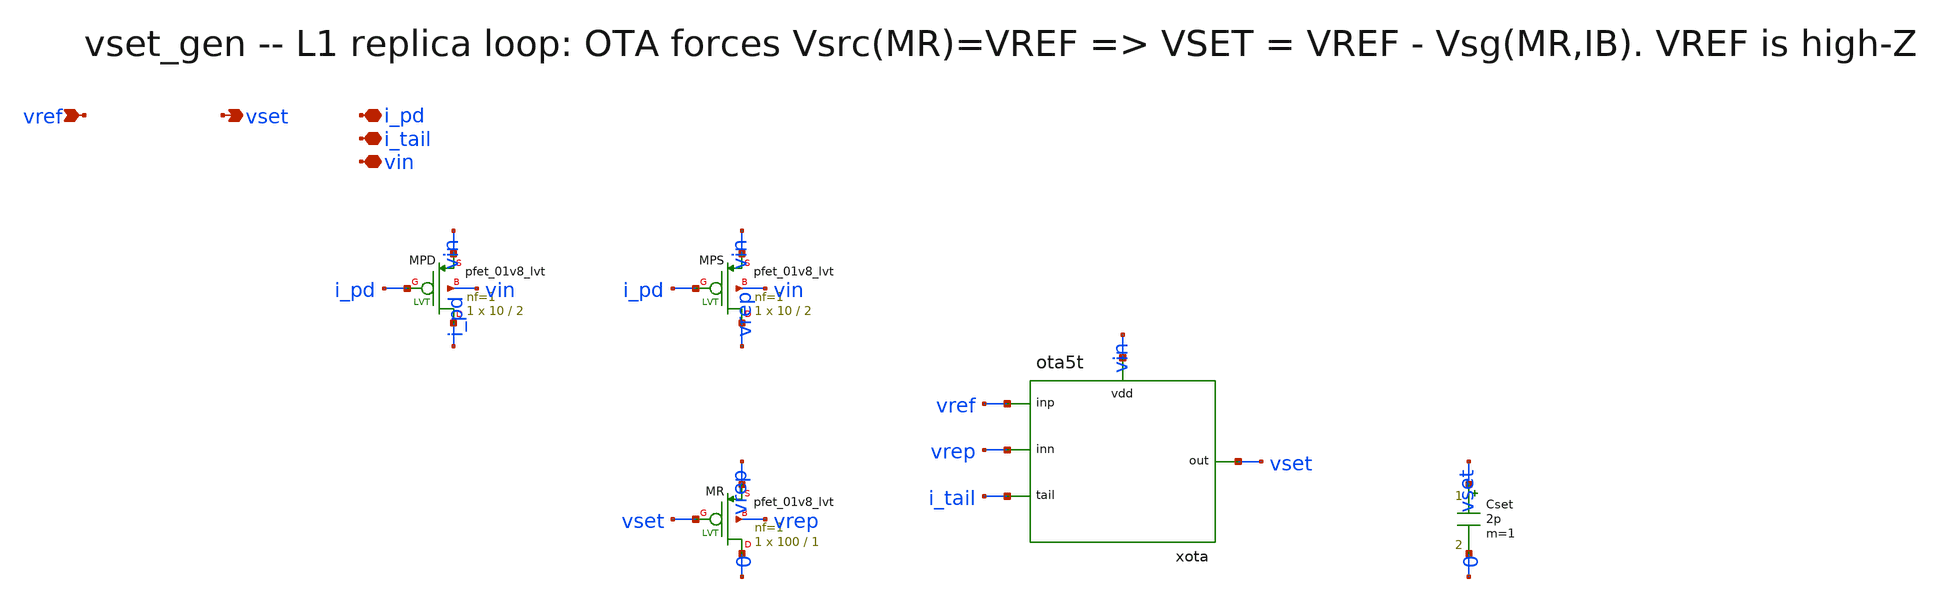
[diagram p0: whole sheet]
** sch_path: xschem/onetops/vset_gen.sch
**.subckt vset_gen vref vset i_pd i_tail vin
*.ipin vref
*.opin vset
*.iopin i_pd
*.iopin i_tail
*.iopin vin
XMPD i_pd i_pd vin vin sky130_fd_pr__pfet_01v8_lvt L=2 W=10 nf=1 ad='int((1 + 1)/2) * 10 / 1 * 0.29'
+ as='int((1 + 2)/2) * 10 / 1 * 0.29' pd='2*int((1 + 1)/2) * (10 / 1 + 0.29)' ps='2*int((1 + 2)/2) * (10 / 1 + 0.29)'
+ nrd='0.29 / 10 ' nrs='0.29 / 10 ' sa=0 sb=0 sd=0 mult=1 m=1
XMPS vrep i_pd vin vin sky130_fd_pr__pfet_01v8_lvt L=2 W=10 nf=1 ad='int((1 + 1)/2) * 10 / 1 * 0.29'
+ as='int((1 + 2)/2) * 10 / 1 * 0.29' pd='2*int((1 + 1)/2) * (10 / 1 + 0.29)' ps='2*int((1 + 2)/2) * (10 / 1 + 0.29)'
+ nrd='0.29 / 10 ' nrs='0.29 / 10 ' sa=0 sb=0 sd=0 mult=1 m=1
XMR 0 vset vrep vrep sky130_fd_pr__pfet_01v8_lvt L=1 W=100 nf=1 ad='int((1 + 1)/2) * 100 / 1 * 0.29'
+ as='int((1 + 2)/2) * 100 / 1 * 0.29' pd='2*int((1 + 1)/2) * (100 / 1 + 0.29)' ps='2*int((1 + 2)/2) * (100 / 1 + 0.29)'
+ nrd='0.29 / 100 ' nrs='0.29 / 100 ' sa=0 sb=0 sd=0 mult=1 m=1
xota vref vrep i_tail vset vin ota5t
Cset vset 0 2p m=1
**.ends

* expanding   symbol:  onetops/ota5t.sym # of pins=5
** sym_path: xschem/onetops/ota5t.sym
** sch_path: xschem/onetops/ota5t.sch
.subckt ota5t inp inn tail out vdd
*.ipin inp
*.ipin inn
*.opin out
*.iopin tail
*.iopin vdd
XMP1 nd nd vdd vdd sky130_fd_pr__pfet_01v8_lvt L=2 W=20 nf=1 ad='int((1 + 1)/2) * 20 / 1 * 0.29' as='int((1 + 2)/2) * 20 / 1 * 0.29'
+ pd='2*int((1 + 1)/2) * (20 / 1 + 0.29)' ps='2*int((1 + 2)/2) * (20 / 1 + 0.29)' nrd='0.29 / 20 ' nrs='0.29 / 20 '
+ sa=0 sb=0 sd=0 mult=1 m=1
XMP2 out nd vdd vdd sky130_fd_pr__pfet_01v8_lvt L=2 W=20 nf=1 ad='int((1 + 1)/2) * 20 / 1 * 0.29' as='int((1 + 2)/2) * 20 / 1 * 0.29'
+ pd='2*int((1 + 1)/2) * (20 / 1 + 0.29)' ps='2*int((1 + 2)/2) * (20 / 1 + 0.29)' nrd='0.29 / 20 ' nrs='0.29 / 20 '
+ sa=0 sb=0 sd=0 mult=1 m=1
XMN1 nd inp tail 0 sky130_fd_pr__nfet_01v8 L=1 W=5 nf=1 ad='int((1 + 1)/2) * 5 / 1 * 0.29' as='int((1 + 2)/2) * 5 / 1 * 0.29'
+ pd='2*int((1 + 1)/2) * (5 / 1 + 0.29)' ps='2*int((1 + 2)/2) * (5 / 1 + 0.29)' nrd='0.29 / 5 ' nrs='0.29 / 5 '
+ sa=0 sb=0 sd=0 mult=1 m=1
XMN2 out inn tail 0 sky130_fd_pr__nfet_01v8 L=1 W=5 nf=1 ad='int((1 + 1)/2) * 5 / 1 * 0.29' as='int((1 + 2)/2) * 5 / 1 * 0.29'
+ pd='2*int((1 + 1)/2) * (5 / 1 + 0.29)' ps='2*int((1 + 2)/2) * (5 / 1 + 0.29)' nrd='0.29 / 5 ' nrs='0.29 / 5 '
+ sa=0 sb=0 sd=0 mult=1 m=1
.ends

.end
